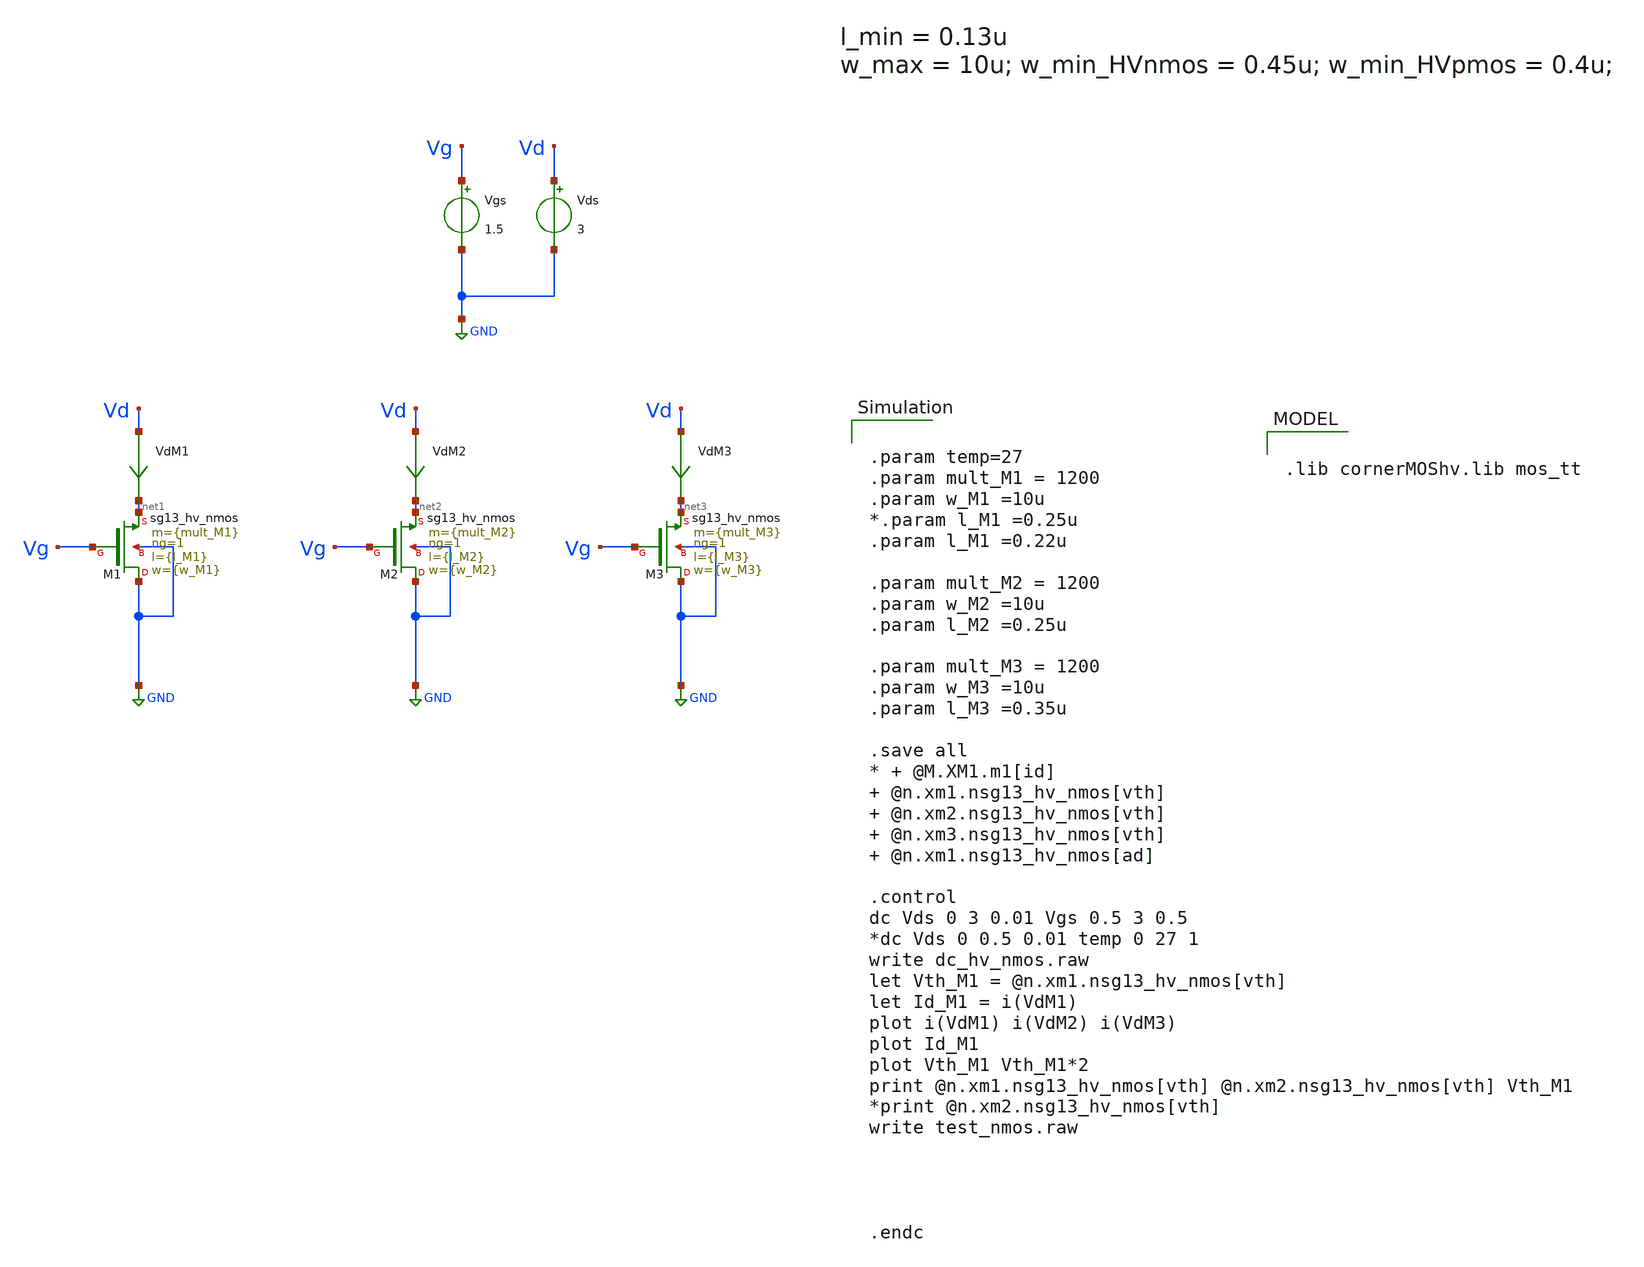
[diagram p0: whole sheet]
** sch_path: xschem/TB_hvNMOS_charact.sch
**.subckt TB_hvNMOS_charact
XM1 GND Vg net1 GND sg13_hv_nmos w={w_M1} l={l_M1} ng=1 m={mult_M1} mm_ok=1
Vgs Vg GND 1.5
Vds Vd GND 3
VdM1 Vd net1 0
.save i(vdm1)
XM2 GND Vg net2 GND sg13_hv_nmos w={w_M2} l={l_M2} ng=1 m={mult_M2} mm_ok=1
VdM2 Vd net2 0
.save i(vdm2)
XM3 GND Vg net3 GND sg13_hv_nmos w={w_M3} l={l_M3} ng=1 m={mult_M3} mm_ok=1
VdM3 Vd net3 0
.save i(vdm3)
**** begin user architecture code


.param temp=27
.param mult_M1 = 1200
.param w_M1 =10u
*.param l_M1 =0.25u
.param l_M1 =0.22u

.param mult_M2 = 1200
.param w_M2 =10u
.param l_M2 =0.25u

.param mult_M3 = 1200
.param w_M3 =10u
.param l_M3 =0.35u

.save all
* + @M.XM1.m1[id]  @n.xm1.nsg13_hv_nmos[vth]  @n.xm2.nsg13_hv_nmos[vth]  @n.xm3.nsg13_hv_nmos[vth]
*+  @n.xm1.nsg13_hv_nmos[ad]

.control
dc Vds 0 3 0.01 Vgs 0.5 3 0.5
*dc Vds 0 0.5 0.01 temp 0 27 1
write dc_hv_nmos.raw
let Vth_M1 = @n.xm1.nsg13_hv_nmos[vth]
let Id_M1 = i(VdM1)
plot i(VdM1) i(VdM2) i(VdM3)
plot Id_M1
plot Vth_M1 Vth_M1*2
print @n.xm1.nsg13_hv_nmos[vth] @n.xm2.nsg13_hv_nmos[vth] Vth_M1
*print @n.xm2.nsg13_hv_nmos[vth]
write test_nmos.raw




.endc



.lib cornerMOShv.lib mos_tt

**** end user architecture code
**.ends
.GLOBAL GND
.end
